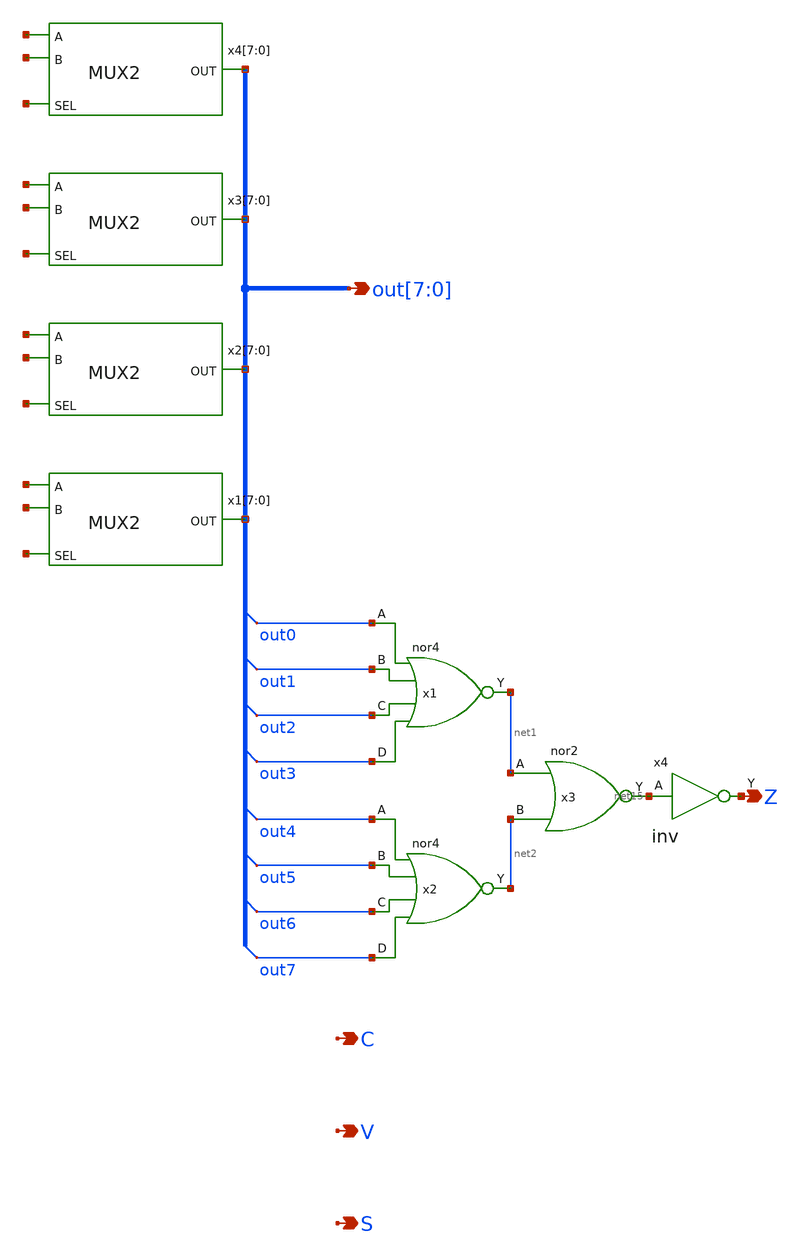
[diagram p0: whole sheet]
** sch_path: design/xschem/opcodemux/opcodemux.sch
**.subckt opcodemux out[7],out[6],out[5],out[4],out[3],out[2],out[1],out[0] Z C V S
*.opin out[7],out[6],out[5],out[4],out[3],out[2],out[1],out[0]
*.opin Z
*.opin C
*.opin V
*.opin S
x1[7] net3[7] net4[7] net5[7] out[7] VSS VDD MUX2
x1[6] net3[6] net4[6] net5[6] out[6] VSS VDD MUX2
x1[5] net3[5] net4[5] net5[5] out[5] VSS VDD MUX2
x1[4] net3[4] net4[4] net5[4] out[4] VSS VDD MUX2
x1[3] net3[3] net4[3] net5[3] out[3] VSS VDD MUX2
x1[2] net3[2] net4[2] net5[2] out[2] VSS VDD MUX2
x1[1] net3[1] net4[1] net5[1] out[1] VSS VDD MUX2
x1[0] net3[0] net4[0] net5[0] out[0] VSS VDD MUX2
x2[7] net6[7] net7[7] net8[7] out[7] VSS VDD MUX2
x2[6] net6[6] net7[6] net8[6] out[6] VSS VDD MUX2
x2[5] net6[5] net7[5] net8[5] out[5] VSS VDD MUX2
x2[4] net6[4] net7[4] net8[4] out[4] VSS VDD MUX2
x2[3] net6[3] net7[3] net8[3] out[3] VSS VDD MUX2
x2[2] net6[2] net7[2] net8[2] out[2] VSS VDD MUX2
x2[1] net6[1] net7[1] net8[1] out[1] VSS VDD MUX2
x2[0] net6[0] net7[0] net8[0] out[0] VSS VDD MUX2
x3[7] net9[7] net10[7] net11[7] out[7] VSS VDD MUX2
x3[6] net9[6] net10[6] net11[6] out[6] VSS VDD MUX2
x3[5] net9[5] net10[5] net11[5] out[5] VSS VDD MUX2
x3[4] net9[4] net10[4] net11[4] out[4] VSS VDD MUX2
x3[3] net9[3] net10[3] net11[3] out[3] VSS VDD MUX2
x3[2] net9[2] net10[2] net11[2] out[2] VSS VDD MUX2
x3[1] net9[1] net10[1] net11[1] out[1] VSS VDD MUX2
x3[0] net9[0] net10[0] net11[0] out[0] VSS VDD MUX2
x4[7] net12[7] net13[7] net14[7] out[7] VSS VDD MUX2
x4[6] net12[6] net13[6] net14[6] out[6] VSS VDD MUX2
x4[5] net12[5] net13[5] net14[5] out[5] VSS VDD MUX2
x4[4] net12[4] net13[4] net14[4] out[4] VSS VDD MUX2
x4[3] net12[3] net13[3] net14[3] out[3] VSS VDD MUX2
x4[2] net12[2] net13[2] net14[2] out[2] VSS VDD MUX2
x4[1] net12[1] net13[1] net14[1] out[1] VSS VDD MUX2
x4[0] net12[0] net13[0] net14[0] out[0] VSS VDD MUX2
x1 out0 out1 out2 out3 VSS VDD net1 nor4
x2 out4 out5 out6 out7 VSS VDD net2 nor4
x3 net1 net2 VSS VDD net15 nor2
x4 net15 VSS VDD Z inv
**.ends
.end
